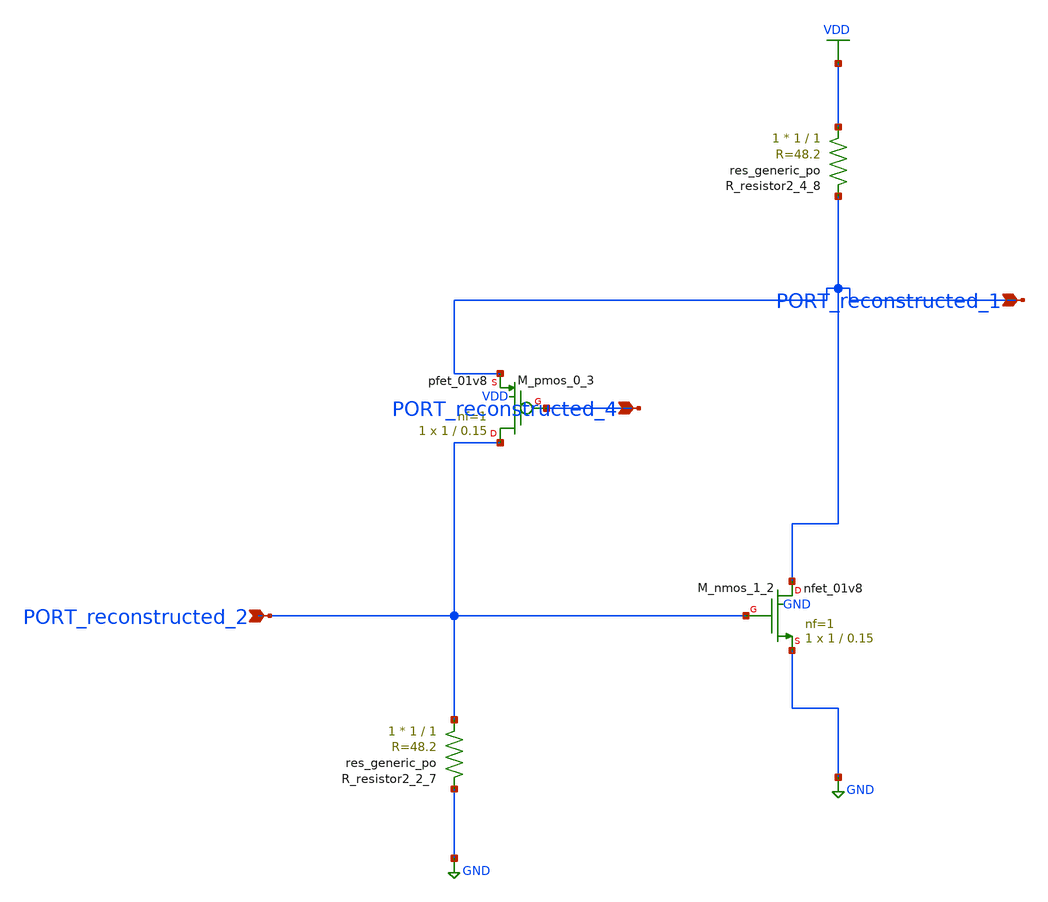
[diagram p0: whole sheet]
** sch_path: schematics/AMSNet/521.sch
**.subckt 521 PORT_reconstructed_4 PORT_reconstructed_2 PORT_reconstructed_1
*.ipin PORT_reconstructed_4
*.ipin PORT_reconstructed_2
*.ipin PORT_reconstructed_1
XM_nmos_1_2 PORT_reconstructed_1 PORT_reconstructed_2 GND GND sky130_fd_pr__nfet_01v8 L=0.15 W=1 nf=1
+ ad='int((1 + 1)/2) * 1 / 1 * 0.29' as='int((1 + 2)/2) * 1 / 1 * 0.29' pd='2*int((1 + 1)/2) * (1 / 1 + 0.29)'
+ ps='2*int((1 + 2)/2) * (1 / 1 + 0.29)' nrd='0.29 / 1 ' nrs='0.29 / 1 ' sa=0 sb=0 sd=0 mult=1 m=1
XM_pmos_0_3 PORT_reconstructed_2 PORT_reconstructed_4 PORT_reconstructed_1 VDD sky130_fd_pr__pfet_01v8
+ L=0.15 W=1 nf=1 ad='int((1 + 1)/2) * 1 / 1 * 0.29' as='int((1 + 2)/2) * 1 / 1 * 0.29' pd='2*int((1 + 1)/2) * (1 / 1 + 0.29)'
+ ps='2*int((1 + 2)/2) * (1 / 1 + 0.29)' nrd='0.29 / 1 ' nrs='0.29 / 1 ' sa=0 sb=0 sd=0 mult=1 m=1
XR_resistor2_2_7 PORT_reconstructed_2 GND sky130_fd_pr__res_generic_po W=1 L=1 m=1
XR_resistor2_4_8 VDD PORT_reconstructed_1 sky130_fd_pr__res_generic_po W=1 L=1 m=1
**.ends
.GLOBAL GND
.GLOBAL VDD
.end
